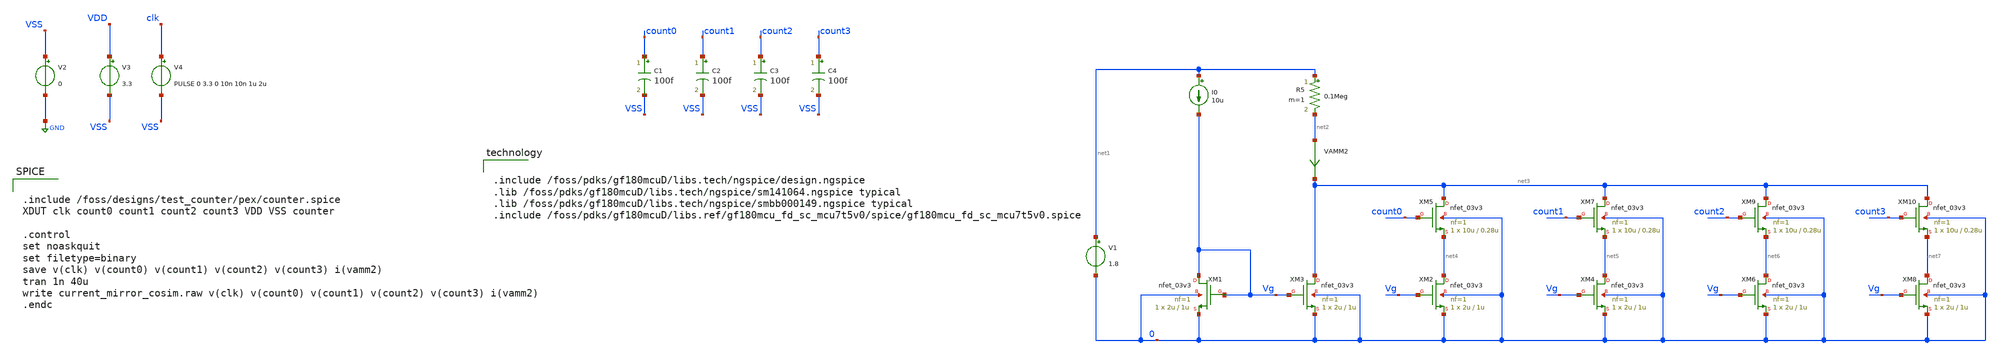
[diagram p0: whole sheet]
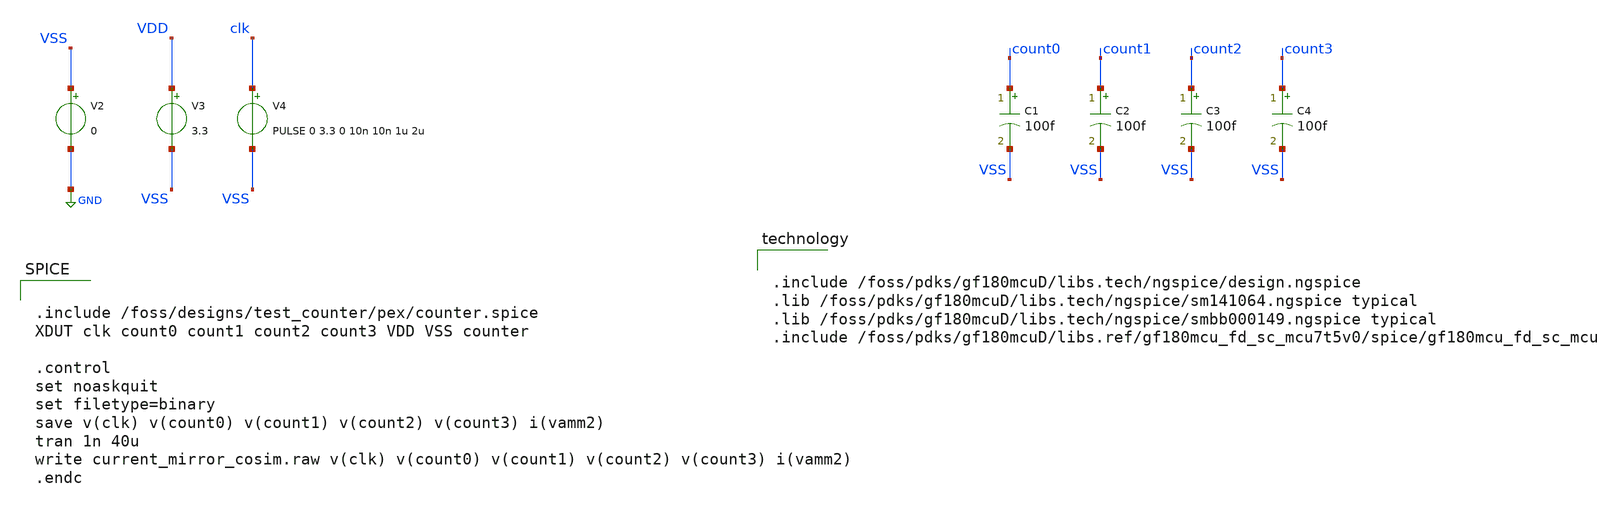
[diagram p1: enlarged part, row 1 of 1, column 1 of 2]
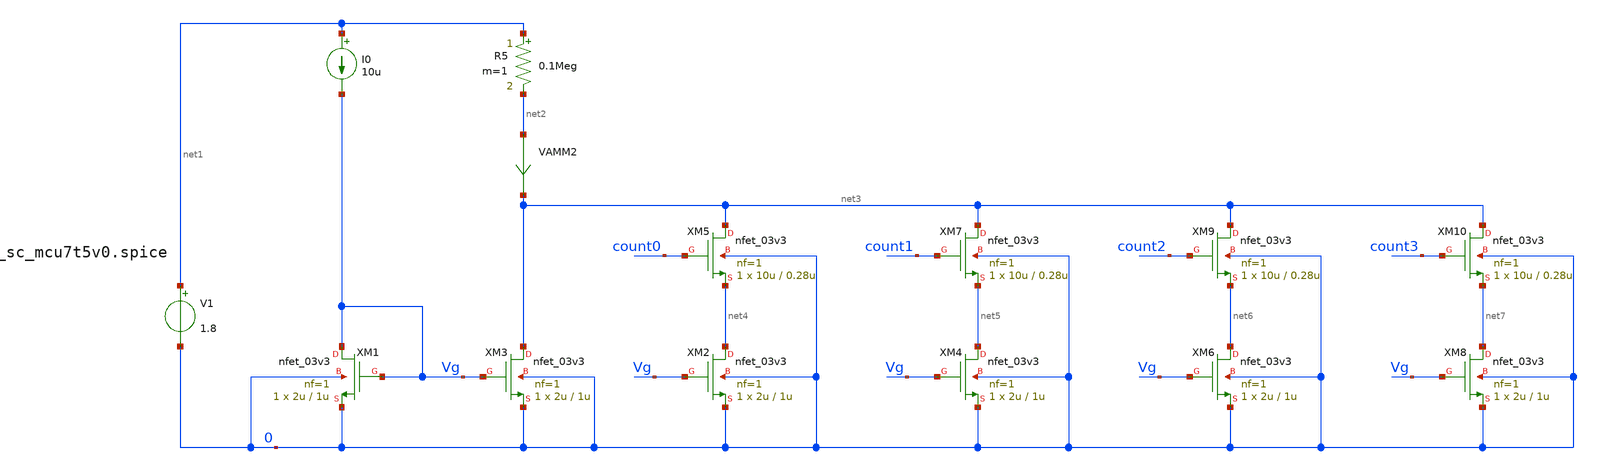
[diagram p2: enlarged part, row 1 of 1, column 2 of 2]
** sch_path: sscs-chipathon-2026/resources/C_MOSbius_playground_for_chips/cosimulation/pex_view/cosimulation/current_mirror_cosim.sch
**.subckt current_mirror_cosim
I0 net1 Vg 10u
V1 net1 0 1.8
R5 net1 net2 0.1Meg m=1
VAMM2 net2 net3 0
XM3 net3 Vg 0 0 nfet_03v3 L=1u W=2u nf=1 ad='int((nf+1)/2) * W/nf * 0.18u' as='int((nf+2)/2) * W/nf * 0.18u'
+ pd='2*int((nf+1)/2) * (W/nf + 0.18u)' ps='2*int((nf+2)/2) * (W/nf + 0.18u)' nrd='0.18u / W' nrs='0.18u / W'
+ sa=0 sb=0 sd=0 m=1
XM1 Vg Vg 0 0 nfet_03v3 L=1u W=2u nf=1 ad='int((nf+1)/2) * W/nf * 0.18u' as='int((nf+2)/2) * W/nf * 0.18u'
+ pd='2*int((nf+1)/2) * (W/nf + 0.18u)' ps='2*int((nf+2)/2) * (W/nf + 0.18u)' nrd='0.18u / W' nrs='0.18u / W'
+ sa=0 sb=0 sd=0 m=1
XM2 net4 Vg 0 0 nfet_03v3 L=1u W=2u nf=1 ad='int((nf+1)/2) * W/nf * 0.18u' as='int((nf+2)/2) * W/nf * 0.18u'
+ pd='2*int((nf+1)/2) * (W/nf + 0.18u)' ps='2*int((nf+2)/2) * (W/nf + 0.18u)' nrd='0.18u / W' nrs='0.18u / W'
+ sa=0 sb=0 sd=0 m=1
XM4 net5 Vg 0 0 nfet_03v3 L=1u W=2u nf=1 ad='int((nf+1)/2) * W/nf * 0.18u' as='int((nf+2)/2) * W/nf * 0.18u'
+ pd='2*int((nf+1)/2) * (W/nf + 0.18u)' ps='2*int((nf+2)/2) * (W/nf + 0.18u)' nrd='0.18u / W' nrs='0.18u / W'
+ sa=0 sb=0 sd=0 m=1
XM6 net6 Vg 0 0 nfet_03v3 L=1u W=2u nf=1 ad='int((nf+1)/2) * W/nf * 0.18u' as='int((nf+2)/2) * W/nf * 0.18u'
+ pd='2*int((nf+1)/2) * (W/nf + 0.18u)' ps='2*int((nf+2)/2) * (W/nf + 0.18u)' nrd='0.18u / W' nrs='0.18u / W'
+ sa=0 sb=0 sd=0 m=1
XM8 net7 Vg 0 0 nfet_03v3 L=1u W=2u nf=1 ad='int((nf+1)/2) * W/nf * 0.18u' as='int((nf+2)/2) * W/nf * 0.18u'
+ pd='2*int((nf+1)/2) * (W/nf + 0.18u)' ps='2*int((nf+2)/2) * (W/nf + 0.18u)' nrd='0.18u / W' nrs='0.18u / W'
+ sa=0 sb=0 sd=0 m=1
XM5 net3 count0 net4 0 nfet_03v3 L=0.28u W=10u nf=1 ad='int((nf+1)/2) * W/nf * 0.18u' as='int((nf+2)/2) * W/nf * 0.18u'
+ pd='2*int((nf+1)/2) * (W/nf + 0.18u)' ps='2*int((nf+2)/2) * (W/nf + 0.18u)' nrd='0.18u / W' nrs='0.18u / W'
+ sa=0 sb=0 sd=0 m=1
XM7 net3 count1 net5 0 nfet_03v3 L=0.28u W=10u nf=1 ad='int((nf+1)/2) * W/nf * 0.18u' as='int((nf+2)/2) * W/nf * 0.18u'
+ pd='2*int((nf+1)/2) * (W/nf + 0.18u)' ps='2*int((nf+2)/2) * (W/nf + 0.18u)' nrd='0.18u / W' nrs='0.18u / W'
+ sa=0 sb=0 sd=0 m=1
XM9 net3 count2 net6 0 nfet_03v3 L=0.28u W=10u nf=1 ad='int((nf+1)/2) * W/nf * 0.18u' as='int((nf+2)/2) * W/nf * 0.18u'
+ pd='2*int((nf+1)/2) * (W/nf + 0.18u)' ps='2*int((nf+2)/2) * (W/nf + 0.18u)' nrd='0.18u / W' nrs='0.18u / W'
+ sa=0 sb=0 sd=0 m=1
XM10 net3 count3 net7 0 nfet_03v3 L=0.28u W=10u nf=1 ad='int((nf+1)/2) * W/nf * 0.18u' as='int((nf+2)/2) * W/nf * 0.18u'
+ pd='2*int((nf+1)/2) * (W/nf + 0.18u)' ps='2*int((nf+2)/2) * (W/nf + 0.18u)' nrd='0.18u / W' nrs='0.18u / W'
+ sa=0 sb=0 sd=0 m=1
V2 VSS GND 0
V3 VDD VSS 3.3
V4 clk VSS PULSE 0 3.3 0 10n 10n 1u 2u
C1 count0 VSS 100f m=1
C2 count1 VSS 100f m=1
C3 count2 VSS 100f m=1
C4 count3 VSS 100f m=1
**** begin user architecture code


.include /foss/designs/test_counter/pex/counter.spice
XDUT clk count0 count1 count2 count3 VDD VSS counter

.control
set noaskquit
set filetype=binary
save v(clk) v(count0) v(count1) v(count2) v(count3) i(vamm2)
tran 1n 40u
write current_mirror_cosim.raw v(clk) v(count0) v(count1) v(count2) v(count3) i(vamm2)
.endc




.include /foss/pdks/gf180mcuD/libs.tech/ngspice/design.ngspice
.lib /foss/pdks/gf180mcuD/libs.tech/ngspice/sm141064.ngspice typical
.lib /foss/pdks/gf180mcuD/libs.tech/ngspice/smbb000149.ngspice typical
.include /foss/pdks/gf180mcuD/libs.ref/gf180mcu_fd_sc_mcu7t5v0/spice/gf180mcu_fd_sc_mcu7t5v0.spice


**** end user architecture code
**.ends
.GLOBAL GND
.end
